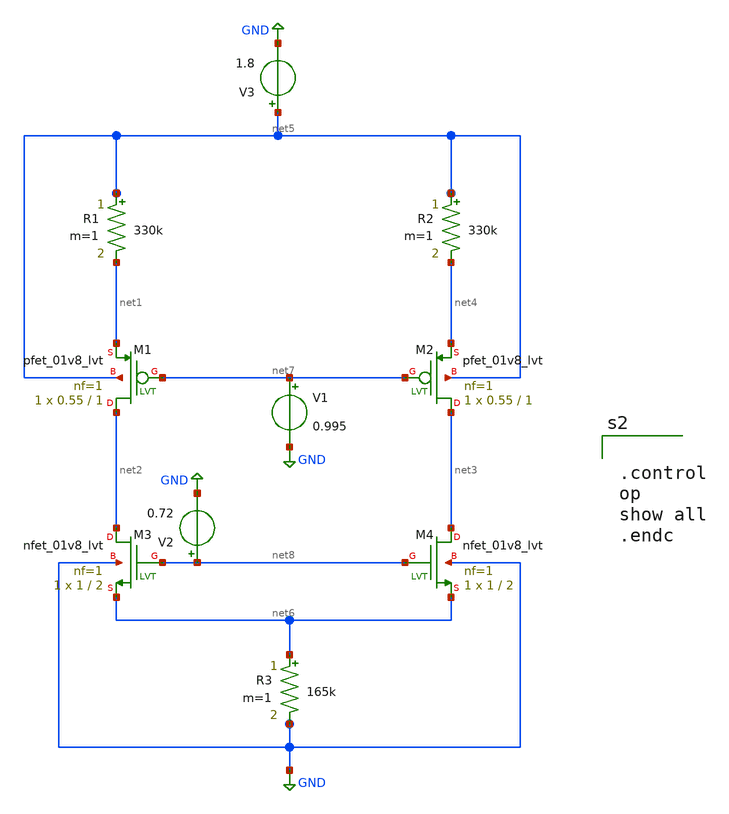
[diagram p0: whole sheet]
** sch_path: untitled-3.sch
**.subckt untitled-3
XM1 net2 net7 net1 net5 sky130_fd_pr__pfet_01v8_lvt L=1 W=0.55 nf=1 ad='int((nf+1)/2) * W/nf * 0.29'
+ as='int((nf+2)/2) * W/nf * 0.29' pd='2*int((nf+1)/2) * (W/nf + 0.29)' ps='2*int((nf+2)/2) * (W/nf + 0.29)'
+ nrd='0.29 / W' nrs='0.29 / W' sa=0 sb=0 sd=0 mult=1 m=1
XM2 net3 net7 net4 net5 sky130_fd_pr__pfet_01v8_lvt L=1 W=0.55 nf=1 ad='int((nf+1)/2) * W/nf * 0.29'
+ as='int((nf+2)/2) * W/nf * 0.29' pd='2*int((nf+1)/2) * (W/nf + 0.29)' ps='2*int((nf+2)/2) * (W/nf + 0.29)'
+ nrd='0.29 / W' nrs='0.29 / W' sa=0 sb=0 sd=0 mult=1 m=1
XM3 net2 net8 net6 GND sky130_fd_pr__nfet_01v8_lvt L=2 W=1 nf=1 ad='int((nf+1)/2) * W/nf * 0.29' as='int((nf+2)/2) * W/nf * 0.29'
+ pd='2*int((nf+1)/2) * (W/nf + 0.29)' ps='2*int((nf+2)/2) * (W/nf + 0.29)' nrd='0.29 / W' nrs='0.29 / W'
+ sa=0 sb=0 sd=0 mult=1 m=1
XM4 net3 net8 net6 GND sky130_fd_pr__nfet_01v8_lvt L=2 W=1 nf=1 ad='int((nf+1)/2) * W/nf * 0.29' as='int((nf+2)/2) * W/nf * 0.29'
+ pd='2*int((nf+1)/2) * (W/nf + 0.29)' ps='2*int((nf+2)/2) * (W/nf + 0.29)' nrd='0.29 / W' nrs='0.29 / W'
+ sa=0 sb=0 sd=0 mult=1 m=1
R1 net5 net1 330k m=1
R2 net5 net4 330k m=1
R3 net6 GND 165k m=1
V1 net7 GND 0.995
V2 net8 GND 0.72
V3 net5 GND 1.8
**** begin user architecture code


.control
op
show all
.endc


*.lib ~/open_pdks/sky130/sky130A/libs.tech/ngspice/sky130.lib.spice tt
.param mc_mm_switch=0
.param mc_pr_switch=0

.include ~/open_pdks/sky130/sky130A/libs.tech/ngspice/corners/tt/nonfet.spice


*model
.include ~/open_pdks/sky130/sky130A/libs.tech/ngspice/all.spice

*mosfet
.include ~/open_pdks/sky130/sky130A/libs.ref/sky130_fd_pr/spice/sky130_fd_pr__pfet_01v8_lvt__tt.corner.spice
.inclued ~/open_pdks/sky130/sky130A/libs.ref/sky130_fd_pr/spice/sky130_fd_pr__nfet_01v8_lvt__tt.corner.spice

*mismatch parameters
.include ~/open_pdks/sky130/sky130A/libs.ref/sky130_fd_pr/spice/sky130_fd_pr__pfet_01v8_lvt__mismatch.corner.spice
.include ~/open_pdks/sky130/sky130A/libs.ref/sky130_fd_pr/spice/sky130_fd_pr__nfet_01v8_lvt__mismatch.corner.spice

**** end user architecture code
**.ends
.GLOBAL GND
.end
